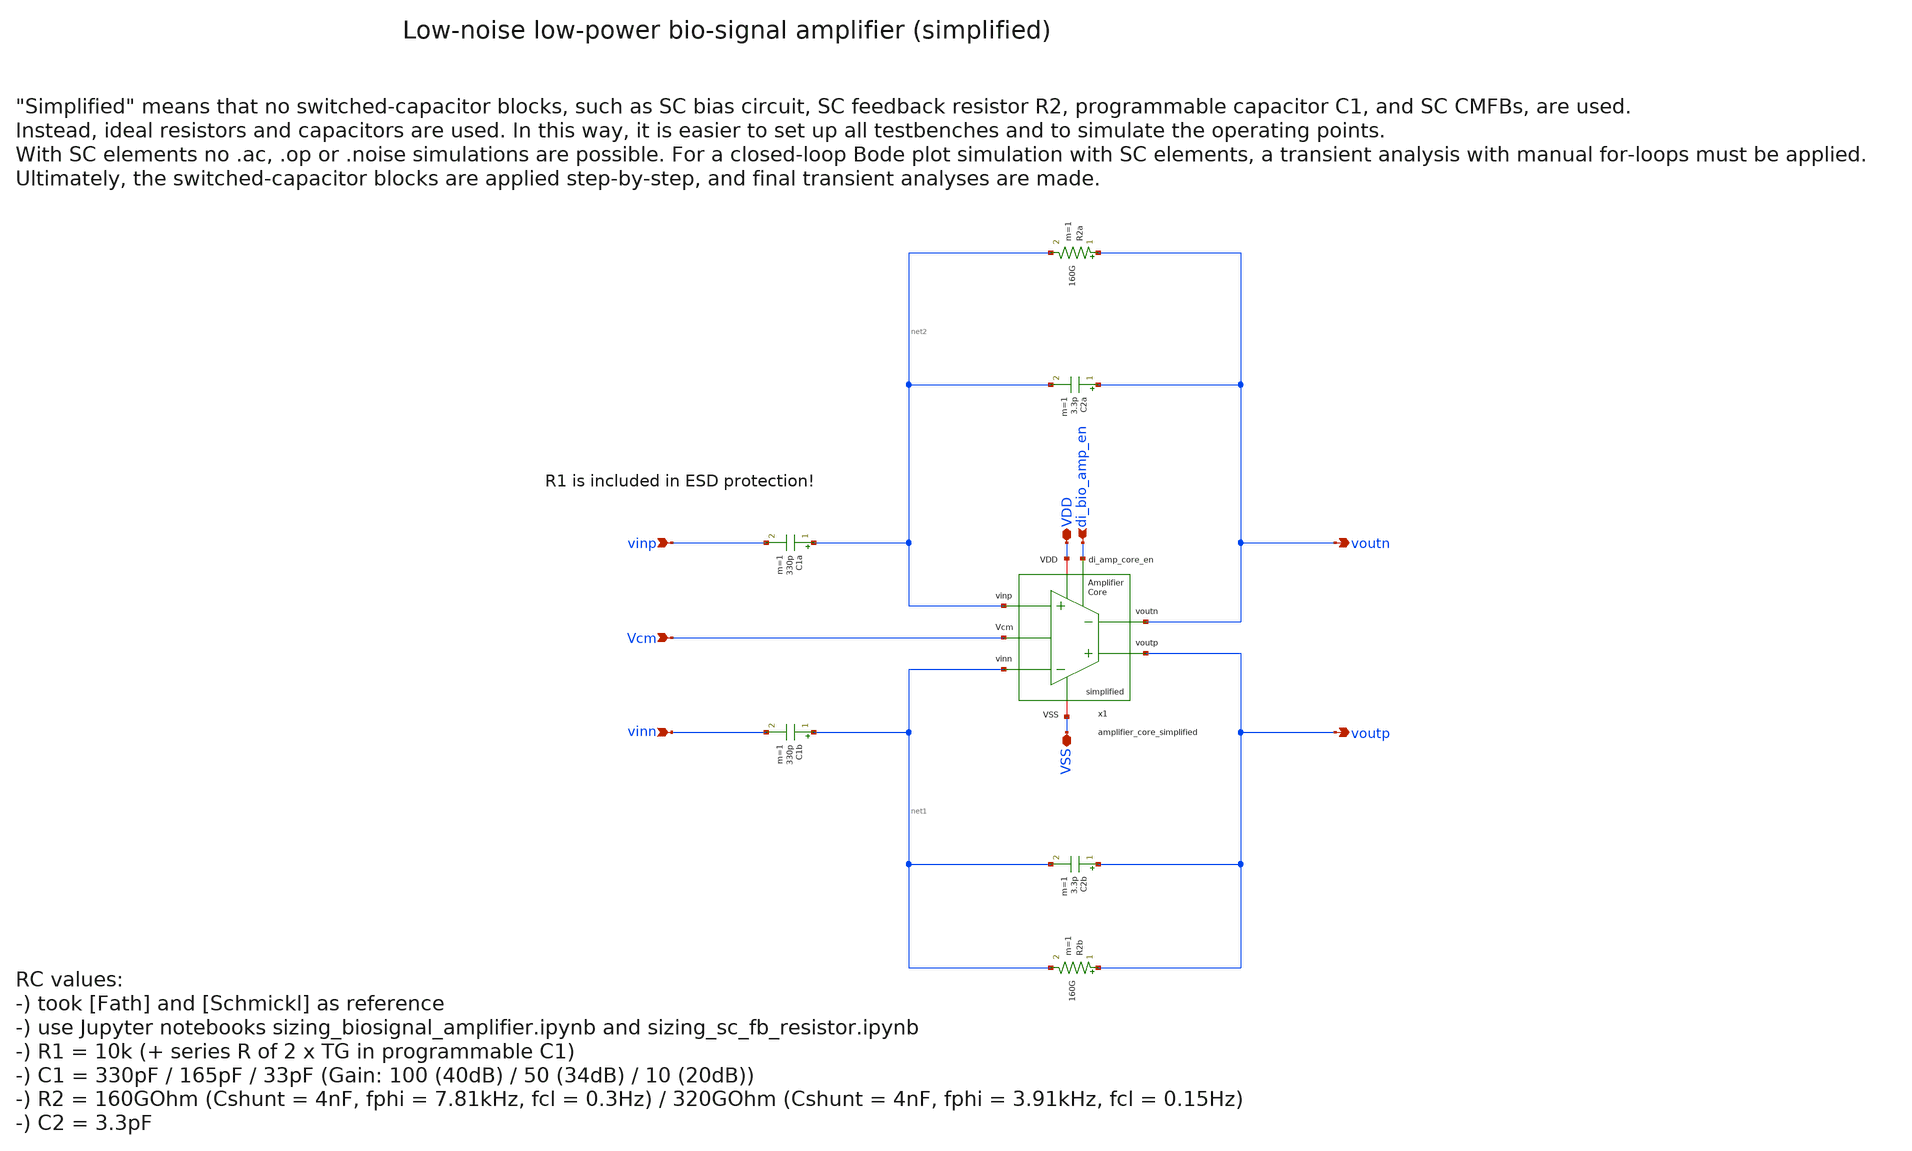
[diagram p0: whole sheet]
** sch_path: SG13G2_ATBS-ADC-main/xschem/bio_amplifier/bio_amplifier_simplified_CACE.sch
**.subckt bio_amplifier_simplified_CACE VDD VSS voutp vinp vinn voutn di_bio_amp_en Vcm
*.iopin VDD
*.iopin VSS
*.opin voutp
*.ipin vinp
*.ipin vinn
*.opin voutn
*.ipin di_bio_amp_en
*.ipin Vcm
R2a voutn net2 160G m=1
R2b voutp net1 160G m=1
C2a voutn net2 3.3p m=1
C2b voutp net1 3.3p m=1
C1a net2 vinp 330p m=1
C1b net1 vinn 330p m=1
x1 voutp voutn di_bio_amp_en net1 net2 VDD VSS Vcm amplifier_core_simplified
**.ends
.end
